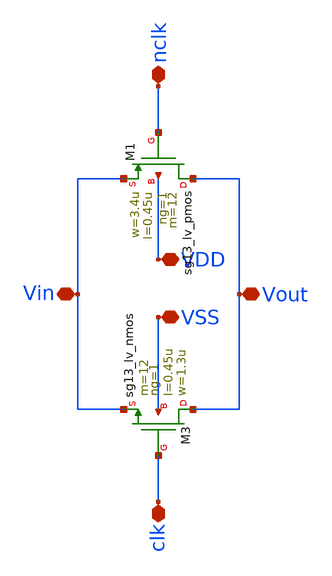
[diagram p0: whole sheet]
** sch_path: unic_cass_wrapper_user_project/ROs_reliability/tgate_force10.sch
**.subckt tgate_force10 nclk clk VDD VSS Vout Vin
*.iopin nclk
*.iopin clk
*.iopin VDD
*.iopin VSS
*.iopin Vout
*.iopin Vin
XM1 Vout nclk Vin VDD sg13_lv_pmos w=3.4u l=0.45u ng=1 m=12 mm_ok=1
XM3 Vout clk Vin VSS sg13_lv_nmos w=1.3u l=0.45u ng=1 m=12 mm_ok=1
**.ends
.end
